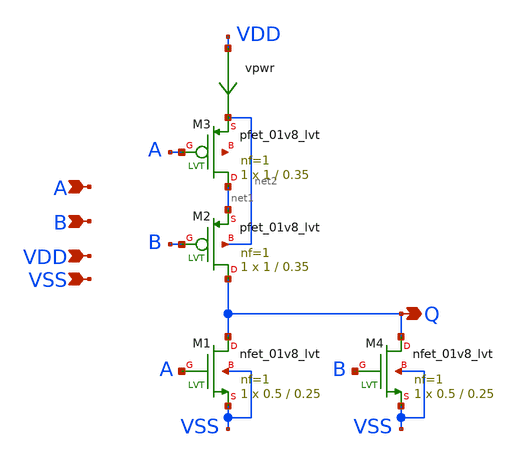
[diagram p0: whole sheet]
** sch_path: xschem/pll_nor.sch
**.subckt pll_nor Q A B VDD VSS
*.opin Q
*.ipin A
*.ipin B
*.ipin VDD
*.ipin VSS
XM3 net1 A net2 net3 sky130_fd_pr__pfet_01v8_lvt L=0.35 W=1 nf=1 ad='int((nf+1)/2) * W/nf * 0.29' as='int((nf+2)/2) * W/nf * 0.29'
+ pd='2*int((nf+1)/2) * (W/nf + 0.29)' ps='2*int((nf+2)/2) * (W/nf + 0.29)' nrd='0.29 / W' nrs='0.29 / W'
+ sa=0 sb=0 sd=0 mult=1 m=1
vpwr VDD net2 0
.save i(vpwr)
XM1 Q A VSS VSS sky130_fd_pr__nfet_01v8_lvt L=0.25 W=0.5 nf=1 ad='int((nf+1)/2) * W/nf * 0.29' as='int((nf+2)/2) * W/nf * 0.29'
+ pd='2*int((nf+1)/2) * (W/nf + 0.29)' ps='2*int((nf+2)/2) * (W/nf + 0.29)' nrd='0.29 / W' nrs='0.29 / W'
+ sa=0 sb=0 sd=0 mult=1 m=1
XM2 Q B net1 net2 sky130_fd_pr__pfet_01v8_lvt L=0.35 W=1 nf=1 ad='int((nf+1)/2) * W/nf * 0.29' as='int((nf+2)/2) * W/nf * 0.29'
+ pd='2*int((nf+1)/2) * (W/nf + 0.29)' ps='2*int((nf+2)/2) * (W/nf + 0.29)' nrd='0.29 / W' nrs='0.29 / W'
+ sa=0 sb=0 sd=0 mult=1 m=1
XM4 Q B VSS VSS sky130_fd_pr__nfet_01v8_lvt L=0.25 W=0.5 nf=1 ad='int((nf+1)/2) * W/nf * 0.29' as='int((nf+2)/2) * W/nf * 0.29'
+ pd='2*int((nf+1)/2) * (W/nf + 0.29)' ps='2*int((nf+2)/2) * (W/nf + 0.29)' nrd='0.29 / W' nrs='0.29 / W'
+ sa=0 sb=0 sd=0 mult=1 m=1
**.ends
.end
